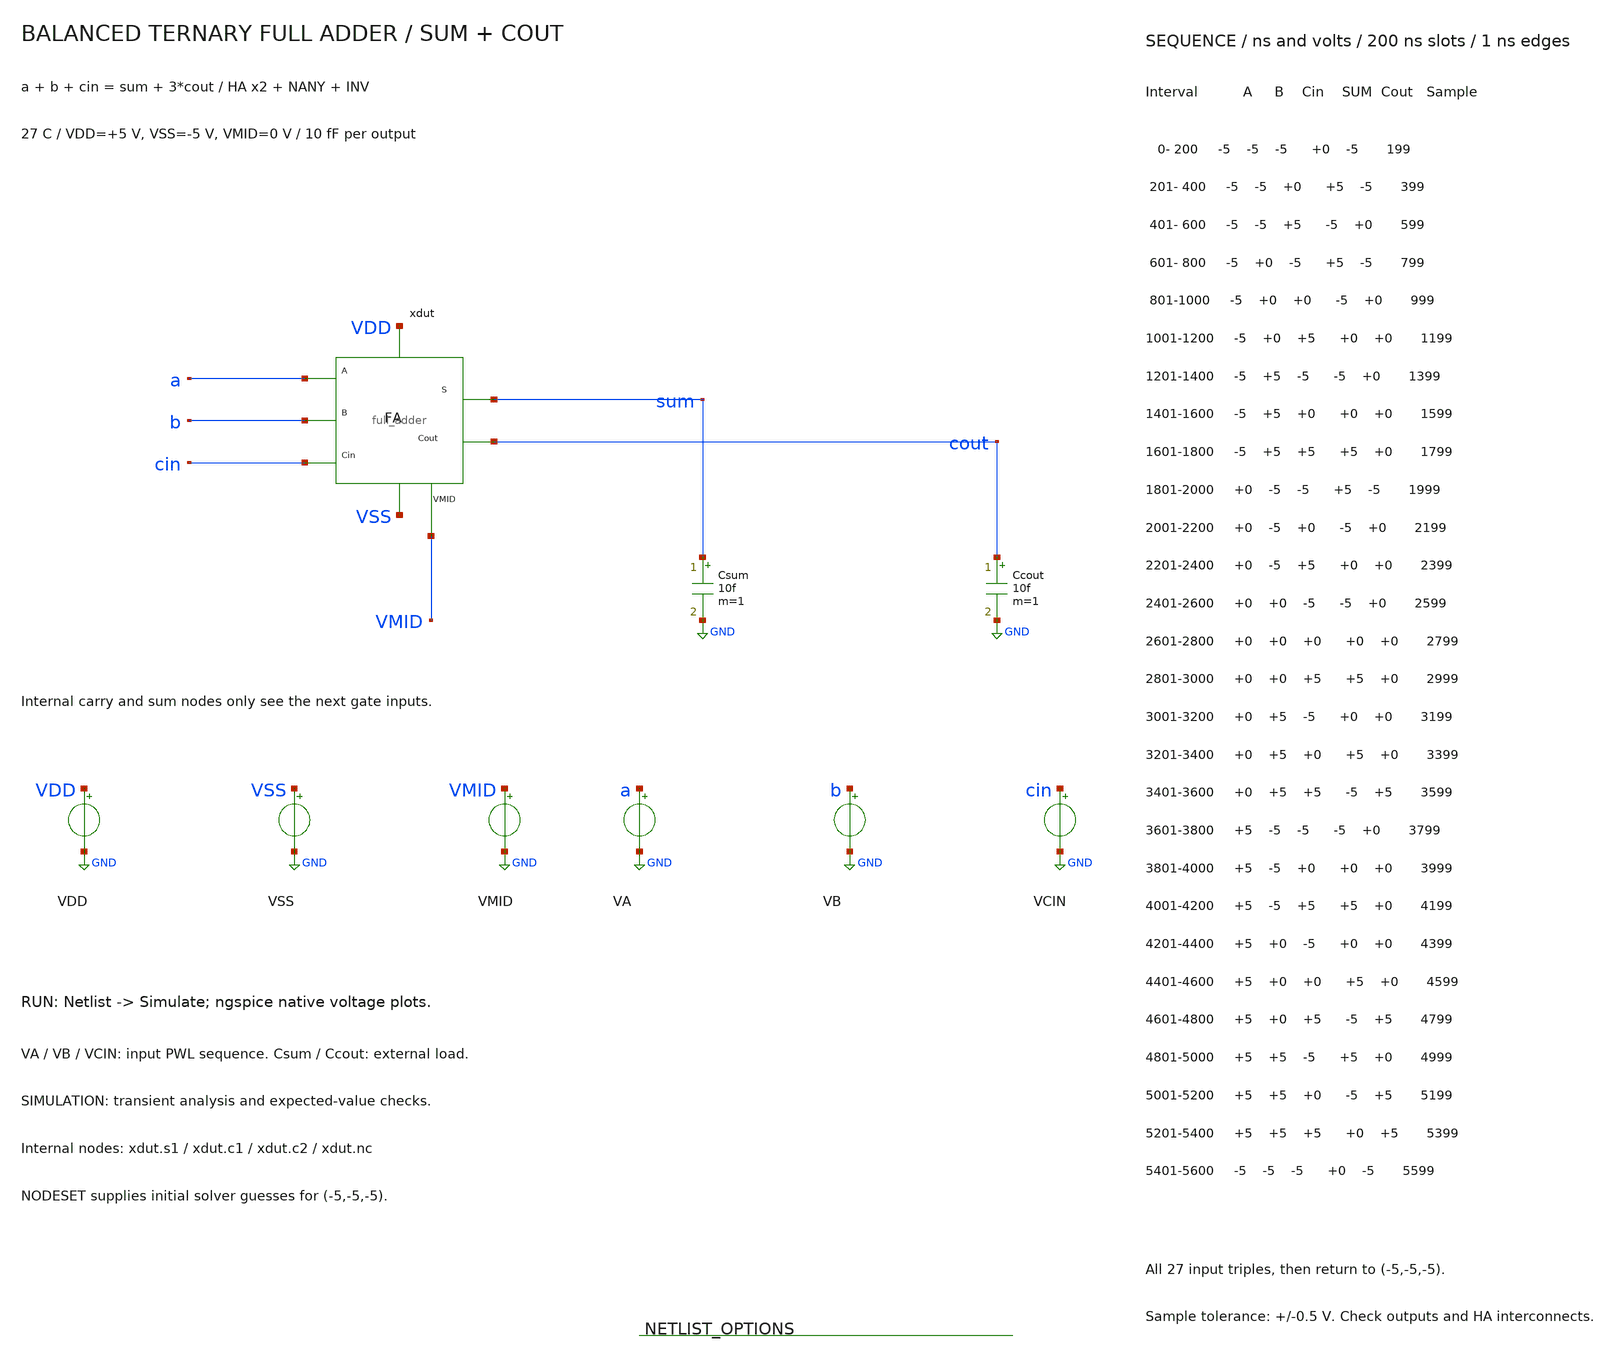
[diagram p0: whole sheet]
** sch_path: member_project/balanced-ternary-logic/PenguinEino/full_adder_tb.sch
**.subckt full_adder_tb
xdut a b cin sum cout VDD VSS VMID full_adder
Csum sum GND 10f m=1
Ccout cout GND 10f m=1
VDD VDD GND 5
VSS VSS GND -5
VMID VMID GND 0
VA a GND PWL(0 -5 200n -5 201n -5 400n -5 401n -5 600n -5 601n -5 800n -5 801n -5 1000n -5 1001n -5
+ 1200n -5 1201n -5 1400n -5 1401n -5 1600n -5 1601n -5 1800n -5 1801n 0 2000n 0 2001n 0 2200n 0 2201n 0
+ 2400n 0 2401n 0 2600n 0 2601n 0 2800n 0 2801n 0 3000n 0 3001n 0 3200n 0 3201n 0 3400n 0 3401n 0 3600n 0
+ 3601n 5 3800n 5 3801n 5 4000n 5 4001n 5 4200n 5 4201n 5 4400n 5 4401n 5 4600n 5 4601n 5 4800n 5 4801n 5
+ 5000n 5 5001n 5 5200n 5 5201n 5 5400n 5 5401n -5 5600n -5)
VB b GND PWL(0 -5 200n -5 201n -5 400n -5 401n -5 600n -5 601n 0 800n 0 801n 0 1000n 0 1001n 0 1200n
+ 0 1201n 5 1400n 5 1401n 5 1600n 5 1601n 5 1800n 5 1801n -5 2000n -5 2001n -5 2200n -5 2201n -5 2400n
+ -5 2401n 0 2600n 0 2601n 0 2800n 0 2801n 0 3000n 0 3001n 5 3200n 5 3201n 5 3400n 5 3401n 5 3600n 5
+ 3601n -5 3800n -5 3801n -5 4000n -5 4001n -5 4200n -5 4201n 0 4400n 0 4401n 0 4600n 0 4601n 0 4800n 0
+ 4801n 5 5000n 5 5001n 5 5200n 5 5201n 5 5400n 5 5401n -5 5600n -5)
VCIN cin GND PWL(0 -5 200n -5 201n 0 400n 0 401n 5 600n 5 601n -5 800n -5 801n 0 1000n 0 1001n 5
+ 1200n 5 1201n -5 1400n -5 1401n 0 1600n 0 1601n 5 1800n 5 1801n -5 2000n -5 2001n 0 2200n 0 2201n 5 2400n
+ 5 2401n -5 2600n -5 2601n 0 2800n 0 2801n 5 3000n 5 3001n -5 3200n -5 3201n 0 3400n 0 3401n 5 3600n 5
+ 3601n -5 3800n -5 3801n 0 4000n 0 4001n 5 4200n 5 4201n -5 4400n -5 4401n 0 4600n 0 4601n 5 4800n 5 4801n
+ -5 5000n -5 5001n 0 5200n 0 5201n 5 5400n 5 5401n -5 5600n -5)
**** begin user architecture code
 .include $::LIB/ip62_models

.temp 27
.options rshunt=1e12
.nodeset v(xdut.s1)=5 v(xdut.c1)=-5 v(xdut.c2)=0 v(xdut.nc)=5 v(sum)=0 v(cout)=-5
.nodeset v(xdut.x_ha1.t)=5 v(xdut.x_ha1.u)=0 v(xdut.x_ha1.na)=5 v(xdut.x_ha1.d)=0 v(xdut.x_ha1.nd)=0
.nodeset v(xdut.x_ha1.x_t.net1)=5 v(xdut.x_ha1.x_t.net2)=5 v(xdut.x_ha1.x_t.net3)=-5
+ v(xdut.x_ha1.x_t.net4)=-5 v(xdut.x_ha1.x_t.net5)=0 v(xdut.x_ha1.x_t.net6)=0
.nodeset v(xdut.x_ha1.x_u.net1)=5 v(xdut.x_ha1.x_u.net2)=5 v(xdut.x_ha1.x_u.net3)=-5
+ v(xdut.x_ha1.x_u.net4)=-5 v(xdut.x_ha1.x_u.net5)=0 v(xdut.x_ha1.x_u.net6)=0
.nodeset v(xdut.x_ha1.x_c.net1)=5 v(xdut.x_ha1.x_c.net2)=5 v(xdut.x_ha1.x_c.net3)=-5
+ v(xdut.x_ha1.x_c.net4)=-5 v(xdut.x_ha1.x_c.net5)=0 v(xdut.x_ha1.x_c.net6)=0
.nodeset v(xdut.x_ha1.x_d.net1)=5 v(xdut.x_ha1.x_d.net2)=5 v(xdut.x_ha1.x_d.net3)=-5
+ v(xdut.x_ha1.x_d.net4)=-5 v(xdut.x_ha1.x_d.net5)=0 v(xdut.x_ha1.x_d.net6)=0
.nodeset v(xdut.x_ha1.x_s.net1)=5 v(xdut.x_ha1.x_s.net2)=5 v(xdut.x_ha1.x_s.net3)=-5
+ v(xdut.x_ha1.x_s.net4)=-5 v(xdut.x_ha1.x_s.net5)=0 v(xdut.x_ha1.x_s.net6)=0
.nodeset v(xdut.x_ha1.x_na.net1)=5 v(xdut.x_ha1.x_na.net2)=-5
.nodeset v(xdut.x_ha1.x_nd.net1)=5 v(xdut.x_ha1.x_nd.net2)=-5
.nodeset v(xdut.x_ha2.t)=0 v(xdut.x_ha2.u)=5 v(xdut.x_ha2.na)=-5 v(xdut.x_ha2.d)=0
+ v(xdut.x_ha2.nd)=0
.nodeset v(xdut.x_ha2.x_t.net1)=5 v(xdut.x_ha2.x_t.net2)=5 v(xdut.x_ha2.x_t.net3)=-5
+ v(xdut.x_ha2.x_t.net4)=-5 v(xdut.x_ha2.x_t.net5)=0 v(xdut.x_ha2.x_t.net6)=0
.nodeset v(xdut.x_ha2.x_u.net1)=5 v(xdut.x_ha2.x_u.net2)=5 v(xdut.x_ha2.x_u.net3)=-5
+ v(xdut.x_ha2.x_u.net4)=-5 v(xdut.x_ha2.x_u.net5)=0 v(xdut.x_ha2.x_u.net6)=0
.nodeset v(xdut.x_ha2.x_c.net1)=5 v(xdut.x_ha2.x_c.net2)=5 v(xdut.x_ha2.x_c.net3)=-5
+ v(xdut.x_ha2.x_c.net4)=-5 v(xdut.x_ha2.x_c.net5)=0 v(xdut.x_ha2.x_c.net6)=0
.nodeset v(xdut.x_ha2.x_d.net1)=5 v(xdut.x_ha2.x_d.net2)=5 v(xdut.x_ha2.x_d.net3)=-5
+ v(xdut.x_ha2.x_d.net4)=-5 v(xdut.x_ha2.x_d.net5)=0 v(xdut.x_ha2.x_d.net6)=0
.nodeset v(xdut.x_ha2.x_s.net1)=5 v(xdut.x_ha2.x_s.net2)=5 v(xdut.x_ha2.x_s.net3)=-5
+ v(xdut.x_ha2.x_s.net4)=-5 v(xdut.x_ha2.x_s.net5)=0 v(xdut.x_ha2.x_s.net6)=0
.nodeset v(xdut.x_ha2.x_na.net1)=5 v(xdut.x_ha2.x_na.net2)=-5
.nodeset v(xdut.x_ha2.x_nd.net1)=5 v(xdut.x_ha2.x_nd.net2)=-5
.nodeset v(xdut.x_cmerge.net1)=5 v(xdut.x_cmerge.net2)=5 v(xdut.x_cmerge.net3)=-5
+ v(xdut.x_cmerge.net4)=-5 v(xdut.x_cmerge.net5)=0 v(xdut.x_cmerge.net6)=0
.nodeset v(xdut.x_cout.net1)=5 v(xdut.x_cout.net2)=-5
.control
save all
set wr_singlescale
set wr_vecnames
setplot const
let failures=0
tran 0.5n 5600n 0 0.5n
plot v(a) v(b) v(cin) v(sum) ylimit -5.5 5.5 title 'Full Adder SUM'
plot v(a) v(b) v(cin) v(cout) ylimit -5.5 5.5 title 'Full Adder COUT'
wrdata full_adder_tran.txt v(a) v(b) v(cin) v(sum) v(cout) v(xdut.s1) v(xdut.c1) v(xdut.c2)
+ v(xdut.nc)
meas tran tran_00_sum find v(sum) at=199n
if abs(tran_00_sum-(0)) > 0.5
let const.failures=const.failures+1
echo FAIL: tran_00_sum expected 0 V
end
meas tran tran_00_cout find v(cout) at=199n
if abs(tran_00_cout-(-5)) > 0.5
let const.failures=const.failures+1
echo FAIL: tran_00_cout expected -5 V
end
meas tran tran_00_xdut_s1 find v(xdut.s1) at=199n
if abs(tran_00_xdut_s1-(5)) > 0.5
let const.failures=const.failures+1
echo FAIL: tran_00_xdut_s1 expected 5 V
end
meas tran tran_00_xdut_c1 find v(xdut.c1) at=199n
if abs(tran_00_xdut_c1-(-5)) > 0.5
let const.failures=const.failures+1
echo FAIL: tran_00_xdut_c1 expected -5 V
end
meas tran tran_00_xdut_c2 find v(xdut.c2) at=199n
if abs(tran_00_xdut_c2-(0)) > 0.5
let const.failures=const.failures+1
echo FAIL: tran_00_xdut_c2 expected 0 V
end
meas tran tran_00_xdut_nc find v(xdut.nc) at=199n
if abs(tran_00_xdut_nc-(5)) > 0.5
let const.failures=const.failures+1
echo FAIL: tran_00_xdut_nc expected 5 V
end
meas tran tran_01_sum find v(sum) at=399n
if abs(tran_01_sum-(5)) > 0.5
let const.failures=const.failures+1
echo FAIL: tran_01_sum expected 5 V
end
meas tran tran_01_cout find v(cout) at=399n
if abs(tran_01_cout-(-5)) > 0.5
let const.failures=const.failures+1
echo FAIL: tran_01_cout expected -5 V
end
meas tran tran_01_xdut_s1 find v(xdut.s1) at=399n
if abs(tran_01_xdut_s1-(5)) > 0.5
let const.failures=const.failures+1
echo FAIL: tran_01_xdut_s1 expected 5 V
end
meas tran tran_01_xdut_c1 find v(xdut.c1) at=399n
if abs(tran_01_xdut_c1-(-5)) > 0.5
let const.failures=const.failures+1
echo FAIL: tran_01_xdut_c1 expected -5 V
end
meas tran tran_01_xdut_c2 find v(xdut.c2) at=399n
if abs(tran_01_xdut_c2-(0)) > 0.5
let const.failures=const.failures+1
echo FAIL: tran_01_xdut_c2 expected 0 V
end
meas tran tran_01_xdut_nc find v(xdut.nc) at=399n
if abs(tran_01_xdut_nc-(5)) > 0.5
let const.failures=const.failures+1
echo FAIL: tran_01_xdut_nc expected 5 V
end
meas tran tran_02_sum find v(sum) at=599n
if abs(tran_02_sum-(-5)) > 0.5
let const.failures=const.failures+1
echo FAIL: tran_02_sum expected -5 V
end
meas tran tran_02_cout find v(cout) at=599n
if abs(tran_02_cout-(0)) > 0.5
let const.failures=const.failures+1
echo FAIL: tran_02_cout expected 0 V
end
meas tran tran_02_xdut_s1 find v(xdut.s1) at=599n
if abs(tran_02_xdut_s1-(5)) > 0.5
let const.failures=const.failures+1
echo FAIL: tran_02_xdut_s1 expected 5 V
end
meas tran tran_02_xdut_c1 find v(xdut.c1) at=599n
if abs(tran_02_xdut_c1-(-5)) > 0.5
let const.failures=const.failures+1
echo FAIL: tran_02_xdut_c1 expected -5 V
end
meas tran tran_02_xdut_c2 find v(xdut.c2) at=599n
if abs(tran_02_xdut_c2-(5)) > 0.5
let const.failures=const.failures+1
echo FAIL: tran_02_xdut_c2 expected 5 V
end
meas tran tran_02_xdut_nc find v(xdut.nc) at=599n
if abs(tran_02_xdut_nc-(0)) > 0.5
let const.failures=const.failures+1
echo FAIL: tran_02_xdut_nc expected 0 V
end
meas tran tran_03_sum find v(sum) at=799n
if abs(tran_03_sum-(5)) > 0.5
let const.failures=const.failures+1
echo FAIL: tran_03_sum expected 5 V
end
meas tran tran_03_cout find v(cout) at=799n
if abs(tran_03_cout-(-5)) > 0.5
let const.failures=const.failures+1
echo FAIL: tran_03_cout expected -5 V
end
meas tran tran_03_xdut_s1 find v(xdut.s1) at=799n
if abs(tran_03_xdut_s1-(-5)) > 0.5
let const.failures=const.failures+1
echo FAIL: tran_03_xdut_s1 expected -5 V
end
meas tran tran_03_xdut_c1 find v(xdut.c1) at=799n
if abs(tran_03_xdut_c1-(0)) > 0.5
let const.failures=const.failures+1
echo FAIL: tran_03_xdut_c1 expected 0 V
end
meas tran tran_03_xdut_c2 find v(xdut.c2) at=799n
if abs(tran_03_xdut_c2-(-5)) > 0.5
let const.failures=const.failures+1
echo FAIL: tran_03_xdut_c2 expected -5 V
end
meas tran tran_03_xdut_nc find v(xdut.nc) at=799n
if abs(tran_03_xdut_nc-(5)) > 0.5
let const.failures=const.failures+1
echo FAIL: tran_03_xdut_nc expected 5 V
end
meas tran tran_04_sum find v(sum) at=999n
if abs(tran_04_sum-(-5)) > 0.5
let const.failures=const.failures+1
echo FAIL: tran_04_sum expected -5 V
end
meas tran tran_04_cout find v(cout) at=999n
if abs(tran_04_cout-(0)) > 0.5
let const.failures=const.failures+1
echo FAIL: tran_04_cout expected 0 V
end
meas tran tran_04_xdut_s1 find v(xdut.s1) at=999n
if abs(tran_04_xdut_s1-(-5)) > 0.5
let const.failures=const.failures+1
echo FAIL: tran_04_xdut_s1 expected -5 V
end
meas tran tran_04_xdut_c1 find v(xdut.c1) at=999n
if abs(tran_04_xdut_c1-(0)) > 0.5
let const.failures=const.failures+1
echo FAIL: tran_04_xdut_c1 expected 0 V
end
meas tran tran_04_xdut_c2 find v(xdut.c2) at=999n
if abs(tran_04_xdut_c2-(0)) > 0.5
let const.failures=const.failures+1
echo FAIL: tran_04_xdut_c2 expected 0 V
end
meas tran tran_04_xdut_nc find v(xdut.nc) at=999n
if abs(tran_04_xdut_nc-(0)) > 0.5
let const.failures=const.failures+1
echo FAIL: tran_04_xdut_nc expected 0 V
end
meas tran tran_05_sum find v(sum) at=1199n
if abs(tran_05_sum-(0)) > 0.5
let const.failures=const.failures+1
echo FAIL: tran_05_sum expected 0 V
end
meas tran tran_05_cout find v(cout) at=1199n
if abs(tran_05_cout-(0)) > 0.5
let const.failures=const.failures+1
echo FAIL: tran_05_cout expected 0 V
end
meas tran tran_05_xdut_s1 find v(xdut.s1) at=1199n
if abs(tran_05_xdut_s1-(-5)) > 0.5
let const.failures=const.failures+1
echo FAIL: tran_05_xdut_s1 expected -5 V
end
meas tran tran_05_xdut_c1 find v(xdut.c1) at=1199n
if abs(tran_05_xdut_c1-(0)) > 0.5
let const.failures=const.failures+1
echo FAIL: tran_05_xdut_c1 expected 0 V
end
meas tran tran_05_xdut_c2 find v(xdut.c2) at=1199n
if abs(tran_05_xdut_c2-(0)) > 0.5
let const.failures=const.failures+1
echo FAIL: tran_05_xdut_c2 expected 0 V
end
meas tran tran_05_xdut_nc find v(xdut.nc) at=1199n
if abs(tran_05_xdut_nc-(0)) > 0.5
let const.failures=const.failures+1
echo FAIL: tran_05_xdut_nc expected 0 V
end
meas tran tran_06_sum find v(sum) at=1399n
if abs(tran_06_sum-(-5)) > 0.5
let const.failures=const.failures+1
echo FAIL: tran_06_sum expected -5 V
end
meas tran tran_06_cout find v(cout) at=1399n
if abs(tran_06_cout-(0)) > 0.5
let const.failures=const.failures+1
echo FAIL: tran_06_cout expected 0 V
end
meas tran tran_06_xdut_s1 find v(xdut.s1) at=1399n
if abs(tran_06_xdut_s1-(0)) > 0.5
let const.failures=const.failures+1
echo FAIL: tran_06_xdut_s1 expected 0 V
end
meas tran tran_06_xdut_c1 find v(xdut.c1) at=1399n
if abs(tran_06_xdut_c1-(0)) > 0.5
let const.failures=const.failures+1
echo FAIL: tran_06_xdut_c1 expected 0 V
end
meas tran tran_06_xdut_c2 find v(xdut.c2) at=1399n
if abs(tran_06_xdut_c2-(0)) > 0.5
let const.failures=const.failures+1
echo FAIL: tran_06_xdut_c2 expected 0 V
end
meas tran tran_06_xdut_nc find v(xdut.nc) at=1399n
if abs(tran_06_xdut_nc-(0)) > 0.5
let const.failures=const.failures+1
echo FAIL: tran_06_xdut_nc expected 0 V
end
meas tran tran_07_sum find v(sum) at=1599n
if abs(tran_07_sum-(0)) > 0.5
let const.failures=const.failures+1
echo FAIL: tran_07_sum expected 0 V
end
meas tran tran_07_cout find v(cout) at=1599n
if abs(tran_07_cout-(0)) > 0.5
let const.failures=const.failures+1
echo FAIL: tran_07_cout expected 0 V
end
meas tran tran_07_xdut_s1 find v(xdut.s1) at=1599n
if abs(tran_07_xdut_s1-(0)) > 0.5
let const.failures=const.failures+1
echo FAIL: tran_07_xdut_s1 expected 0 V
end
meas tran tran_07_xdut_c1 find v(xdut.c1) at=1599n
if abs(tran_07_xdut_c1-(0)) > 0.5
let const.failures=const.failures+1
echo FAIL: tran_07_xdut_c1 expected 0 V
end
meas tran tran_07_xdut_c2 find v(xdut.c2) at=1599n
if abs(tran_07_xdut_c2-(0)) > 0.5
let const.failures=const.failures+1
echo FAIL: tran_07_xdut_c2 expected 0 V
end
meas tran tran_07_xdut_nc find v(xdut.nc) at=1599n
if abs(tran_07_xdut_nc-(0)) > 0.5
let const.failures=const.failures+1
echo FAIL: tran_07_xdut_nc expected 0 V
end
meas tran tran_08_sum find v(sum) at=1799n
if abs(tran_08_sum-(5)) > 0.5
let const.failures=const.failures+1
echo FAIL: tran_08_sum expected 5 V
end
meas tran tran_08_cout find v(cout) at=1799n
if abs(tran_08_cout-(0)) > 0.5
let const.failures=const.failures+1
echo FAIL: tran_08_cout expected 0 V
end
meas tran tran_08_xdut_s1 find v(xdut.s1) at=1799n
if abs(tran_08_xdut_s1-(0)) > 0.5
let const.failures=const.failures+1
echo FAIL: tran_08_xdut_s1 expected 0 V
end
meas tran tran_08_xdut_c1 find v(xdut.c1) at=1799n
if abs(tran_08_xdut_c1-(0)) > 0.5
let const.failures=const.failures+1
echo FAIL: tran_08_xdut_c1 expected 0 V
end
meas tran tran_08_xdut_c2 find v(xdut.c2) at=1799n
if abs(tran_08_xdut_c2-(0)) > 0.5
let const.failures=const.failures+1
echo FAIL: tran_08_xdut_c2 expected 0 V
end
meas tran tran_08_xdut_nc find v(xdut.nc) at=1799n
if abs(tran_08_xdut_nc-(0)) > 0.5
let const.failures=const.failures+1
echo FAIL: tran_08_xdut_nc expected 0 V
end
meas tran tran_09_sum find v(sum) at=1999n
if abs(tran_09_sum-(5)) > 0.5
let const.failures=const.failures+1
echo FAIL: tran_09_sum expected 5 V
end
meas tran tran_09_cout find v(cout) at=1999n
if abs(tran_09_cout-(-5)) > 0.5
let const.failures=const.failures+1
echo FAIL: tran_09_cout expected -5 V
end
meas tran tran_09_xdut_s1 find v(xdut.s1) at=1999n
if abs(tran_09_xdut_s1-(-5)) > 0.5
let const.failures=const.failures+1
echo FAIL: tran_09_xdut_s1 expected -5 V
end
meas tran tran_09_xdut_c1 find v(xdut.c1) at=1999n
if abs(tran_09_xdut_c1-(0)) > 0.5
let const.failures=const.failures+1
echo FAIL: tran_09_xdut_c1 expected 0 V
end
meas tran tran_09_xdut_c2 find v(xdut.c2) at=1999n
if abs(tran_09_xdut_c2-(-5)) > 0.5
let const.failures=const.failures+1
echo FAIL: tran_09_xdut_c2 expected -5 V
end
meas tran tran_09_xdut_nc find v(xdut.nc) at=1999n
if abs(tran_09_xdut_nc-(5)) > 0.5
let const.failures=const.failures+1
echo FAIL: tran_09_xdut_nc expected 5 V
end
meas tran tran_10_sum find v(sum) at=2199n
if abs(tran_10_sum-(-5)) > 0.5
let const.failures=const.failures+1
echo FAIL: tran_10_sum expected -5 V
end
meas tran tran_10_cout find v(cout) at=2199n
if abs(tran_10_cout-(0)) > 0.5
let const.failures=const.failures+1
echo FAIL: tran_10_cout expected 0 V
end
meas tran tran_10_xdut_s1 find v(xdut.s1) at=2199n
if abs(tran_10_xdut_s1-(-5)) > 0.5
let const.failures=const.failures+1
echo FAIL: tran_10_xdut_s1 expected -5 V
end
meas tran tran_10_xdut_c1 find v(xdut.c1) at=2199n
if abs(tran_10_xdut_c1-(0)) > 0.5
let const.failures=const.failures+1
echo FAIL: tran_10_xdut_c1 expected 0 V
end
meas tran tran_10_xdut_c2 find v(xdut.c2) at=2199n
if abs(tran_10_xdut_c2-(0)) > 0.5
let const.failures=const.failures+1
echo FAIL: tran_10_xdut_c2 expected 0 V
end
meas tran tran_10_xdut_nc find v(xdut.nc) at=2199n
if abs(tran_10_xdut_nc-(0)) > 0.5
let const.failures=const.failures+1
echo FAIL: tran_10_xdut_nc expected 0 V
end
meas tran tran_11_sum find v(sum) at=2399n
if abs(tran_11_sum-(0)) > 0.5
let const.failures=const.failures+1
echo FAIL: tran_11_sum expected 0 V
end
meas tran tran_11_cout find v(cout) at=2399n
if abs(tran_11_cout-(0)) > 0.5
let const.failures=const.failures+1
echo FAIL: tran_11_cout expected 0 V
end
meas tran tran_11_xdut_s1 find v(xdut.s1) at=2399n
if abs(tran_11_xdut_s1-(-5)) > 0.5
let const.failures=const.failures+1
echo FAIL: tran_11_xdut_s1 expected -5 V
end
meas tran tran_11_xdut_c1 find v(xdut.c1) at=2399n
if abs(tran_11_xdut_c1-(0)) > 0.5
let const.failures=const.failures+1
echo FAIL: tran_11_xdut_c1 expected 0 V
end
meas tran tran_11_xdut_c2 find v(xdut.c2) at=2399n
if abs(tran_11_xdut_c2-(0)) > 0.5
let const.failures=const.failures+1
echo FAIL: tran_11_xdut_c2 expected 0 V
end
meas tran tran_11_xdut_nc find v(xdut.nc) at=2399n
if abs(tran_11_xdut_nc-(0)) > 0.5
let const.failures=const.failures+1
echo FAIL: tran_11_xdut_nc expected 0 V
end
meas tran tran_12_sum find v(sum) at=2599n
if abs(tran_12_sum-(-5)) > 0.5
let const.failures=const.failures+1
echo FAIL: tran_12_sum expected -5 V
end
meas tran tran_12_cout find v(cout) at=2599n
if abs(tran_12_cout-(0)) > 0.5
let const.failures=const.failures+1
echo FAIL: tran_12_cout expected 0 V
end
meas tran tran_12_xdut_s1 find v(xdut.s1) at=2599n
if abs(tran_12_xdut_s1-(0)) > 0.5
let const.failures=const.failures+1
echo FAIL: tran_12_xdut_s1 expected 0 V
end
meas tran tran_12_xdut_c1 find v(xdut.c1) at=2599n
if abs(tran_12_xdut_c1-(0)) > 0.5
let const.failures=const.failures+1
echo FAIL: tran_12_xdut_c1 expected 0 V
end
meas tran tran_12_xdut_c2 find v(xdut.c2) at=2599n
if abs(tran_12_xdut_c2-(0)) > 0.5
let const.failures=const.failures+1
echo FAIL: tran_12_xdut_c2 expected 0 V
end
meas tran tran_12_xdut_nc find v(xdut.nc) at=2599n
if abs(tran_12_xdut_nc-(0)) > 0.5
let const.failures=const.failures+1
echo FAIL: tran_12_xdut_nc expected 0 V
end
meas tran tran_13_sum find v(sum) at=2799n
if abs(tran_13_sum-(0)) > 0.5
let const.failures=const.failures+1
echo FAIL: tran_13_sum expected 0 V
end
meas tran tran_13_cout find v(cout) at=2799n
if abs(tran_13_cout-(0)) > 0.5
let const.failures=const.failures+1
echo FAIL: tran_13_cout expected 0 V
end
meas tran tran_13_xdut_s1 find v(xdut.s1) at=2799n
if abs(tran_13_xdut_s1-(0)) > 0.5
let const.failures=const.failures+1
echo FAIL: tran_13_xdut_s1 expected 0 V
end
meas tran tran_13_xdut_c1 find v(xdut.c1) at=2799n
if abs(tran_13_xdut_c1-(0)) > 0.5
let const.failures=const.failures+1
echo FAIL: tran_13_xdut_c1 expected 0 V
end
meas tran tran_13_xdut_c2 find v(xdut.c2) at=2799n
if abs(tran_13_xdut_c2-(0)) > 0.5
let const.failures=const.failures+1
echo FAIL: tran_13_xdut_c2 expected 0 V
end
meas tran tran_13_xdut_nc find v(xdut.nc) at=2799n
if abs(tran_13_xdut_nc-(0)) > 0.5
let const.failures=const.failures+1
echo FAIL: tran_13_xdut_nc expected 0 V
end
meas tran tran_14_sum find v(sum) at=2999n
if abs(tran_14_sum-(5)) > 0.5
let const.failures=const.failures+1
echo FAIL: tran_14_sum expected 5 V
end
meas tran tran_14_cout find v(cout) at=2999n
if abs(tran_14_cout-(0)) > 0.5
let const.failures=const.failures+1
echo FAIL: tran_14_cout expected 0 V
end
meas tran tran_14_xdut_s1 find v(xdut.s1) at=2999n
if abs(tran_14_xdut_s1-(0)) > 0.5
let const.failures=const.failures+1
echo FAIL: tran_14_xdut_s1 expected 0 V
end
meas tran tran_14_xdut_c1 find v(xdut.c1) at=2999n
if abs(tran_14_xdut_c1-(0)) > 0.5
let const.failures=const.failures+1
echo FAIL: tran_14_xdut_c1 expected 0 V
end
meas tran tran_14_xdut_c2 find v(xdut.c2) at=2999n
if abs(tran_14_xdut_c2-(0)) > 0.5
let const.failures=const.failures+1
echo FAIL: tran_14_xdut_c2 expected 0 V
end
meas tran tran_14_xdut_nc find v(xdut.nc) at=2999n
if abs(tran_14_xdut_nc-(0)) > 0.5
let const.failures=const.failures+1
echo FAIL: tran_14_xdut_nc expected 0 V
end
meas tran tran_15_sum find v(sum) at=3199n
if abs(tran_15_sum-(0)) > 0.5
let const.failures=const.failures+1
echo FAIL: tran_15_sum expected 0 V
end
meas tran tran_15_cout find v(cout) at=3199n
if abs(tran_15_cout-(0)) > 0.5
let const.failures=const.failures+1
echo FAIL: tran_15_cout expected 0 V
end
meas tran tran_15_xdut_s1 find v(xdut.s1) at=3199n
if abs(tran_15_xdut_s1-(5)) > 0.5
let const.failures=const.failures+1
echo FAIL: tran_15_xdut_s1 expected 5 V
end
meas tran tran_15_xdut_c1 find v(xdut.c1) at=3199n
if abs(tran_15_xdut_c1-(0)) > 0.5
let const.failures=const.failures+1
echo FAIL: tran_15_xdut_c1 expected 0 V
end
meas tran tran_15_xdut_c2 find v(xdut.c2) at=3199n
if abs(tran_15_xdut_c2-(0)) > 0.5
let const.failures=const.failures+1
echo FAIL: tran_15_xdut_c2 expected 0 V
end
meas tran tran_15_xdut_nc find v(xdut.nc) at=3199n
if abs(tran_15_xdut_nc-(0)) > 0.5
let const.failures=const.failures+1
echo FAIL: tran_15_xdut_nc expected 0 V
end
meas tran tran_16_sum find v(sum) at=3399n
if abs(tran_16_sum-(5)) > 0.5
let const.failures=const.failures+1
echo FAIL: tran_16_sum expected 5 V
end
meas tran tran_16_cout find v(cout) at=3399n
if abs(tran_16_cout-(0)) > 0.5
let const.failures=const.failures+1
echo FAIL: tran_16_cout expected 0 V
end
meas tran tran_16_xdut_s1 find v(xdut.s1) at=3399n
if abs(tran_16_xdut_s1-(5)) > 0.5
let const.failures=const.failures+1
echo FAIL: tran_16_xdut_s1 expected 5 V
end
meas tran tran_16_xdut_c1 find v(xdut.c1) at=3399n
if abs(tran_16_xdut_c1-(0)) > 0.5
let const.failures=const.failures+1
echo FAIL: tran_16_xdut_c1 expected 0 V
end
meas tran tran_16_xdut_c2 find v(xdut.c2) at=3399n
if abs(tran_16_xdut_c2-(0)) > 0.5
let const.failures=const.failures+1
echo FAIL: tran_16_xdut_c2 expected 0 V
end
meas tran tran_16_xdut_nc find v(xdut.nc) at=3399n
if abs(tran_16_xdut_nc-(0)) > 0.5
let const.failures=const.failures+1
echo FAIL: tran_16_xdut_nc expected 0 V
end
meas tran tran_17_sum find v(sum) at=3599n
if abs(tran_17_sum-(-5)) > 0.5
let const.failures=const.failures+1
echo FAIL: tran_17_sum expected -5 V
end
meas tran tran_17_cout find v(cout) at=3599n
if abs(tran_17_cout-(5)) > 0.5
let const.failures=const.failures+1
echo FAIL: tran_17_cout expected 5 V
end
meas tran tran_17_xdut_s1 find v(xdut.s1) at=3599n
if abs(tran_17_xdut_s1-(5)) > 0.5
let const.failures=const.failures+1
echo FAIL: tran_17_xdut_s1 expected 5 V
end
meas tran tran_17_xdut_c1 find v(xdut.c1) at=3599n
if abs(tran_17_xdut_c1-(0)) > 0.5
let const.failures=const.failures+1
echo FAIL: tran_17_xdut_c1 expected 0 V
end
meas tran tran_17_xdut_c2 find v(xdut.c2) at=3599n
if abs(tran_17_xdut_c2-(5)) > 0.5
let const.failures=const.failures+1
echo FAIL: tran_17_xdut_c2 expected 5 V
end
meas tran tran_17_xdut_nc find v(xdut.nc) at=3599n
if abs(tran_17_xdut_nc-(-5)) > 0.5
let const.failures=const.failures+1
echo FAIL: tran_17_xdut_nc expected -5 V
end
meas tran tran_18_sum find v(sum) at=3799n
if abs(tran_18_sum-(-5)) > 0.5
let const.failures=const.failures+1
echo FAIL: tran_18_sum expected -5 V
end
meas tran tran_18_cout find v(cout) at=3799n
if abs(tran_18_cout-(0)) > 0.5
let const.failures=const.failures+1
echo FAIL: tran_18_cout expected 0 V
end
meas tran tran_18_xdut_s1 find v(xdut.s1) at=3799n
if abs(tran_18_xdut_s1-(0)) > 0.5
let const.failures=const.failures+1
echo FAIL: tran_18_xdut_s1 expected 0 V
end
meas tran tran_18_xdut_c1 find v(xdut.c1) at=3799n
if abs(tran_18_xdut_c1-(0)) > 0.5
let const.failures=const.failures+1
echo FAIL: tran_18_xdut_c1 expected 0 V
end
meas tran tran_18_xdut_c2 find v(xdut.c2) at=3799n
if abs(tran_18_xdut_c2-(0)) > 0.5
let const.failures=const.failures+1
echo FAIL: tran_18_xdut_c2 expected 0 V
end
meas tran tran_18_xdut_nc find v(xdut.nc) at=3799n
if abs(tran_18_xdut_nc-(0)) > 0.5
let const.failures=const.failures+1
echo FAIL: tran_18_xdut_nc expected 0 V
end
meas tran tran_19_sum find v(sum) at=3999n
if abs(tran_19_sum-(0)) > 0.5
let const.failures=const.failures+1
echo FAIL: tran_19_sum expected 0 V
end
meas tran tran_19_cout find v(cout) at=3999n
if abs(tran_19_cout-(0)) > 0.5
let const.failures=const.failures+1
echo FAIL: tran_19_cout expected 0 V
end
meas tran tran_19_xdut_s1 find v(xdut.s1) at=3999n
if abs(tran_19_xdut_s1-(0)) > 0.5
let const.failures=const.failures+1
echo FAIL: tran_19_xdut_s1 expected 0 V
end
meas tran tran_19_xdut_c1 find v(xdut.c1) at=3999n
if abs(tran_19_xdut_c1-(0)) > 0.5
let const.failures=const.failures+1
echo FAIL: tran_19_xdut_c1 expected 0 V
end
meas tran tran_19_xdut_c2 find v(xdut.c2) at=3999n
if abs(tran_19_xdut_c2-(0)) > 0.5
let const.failures=const.failures+1
echo FAIL: tran_19_xdut_c2 expected 0 V
end
meas tran tran_19_xdut_nc find v(xdut.nc) at=3999n
if abs(tran_19_xdut_nc-(0)) > 0.5
let const.failures=const.failures+1
echo FAIL: tran_19_xdut_nc expected 0 V
end
meas tran tran_20_sum find v(sum) at=4199n
if abs(tran_20_sum-(5)) > 0.5
let const.failures=const.failures+1
echo FAIL: tran_20_sum expected 5 V
end
meas tran tran_20_cout find v(cout) at=4199n
if abs(tran_20_cout-(0)) > 0.5
let const.failures=const.failures+1
echo FAIL: tran_20_cout expected 0 V
end
meas tran tran_20_xdut_s1 find v(xdut.s1) at=4199n
if abs(tran_20_xdut_s1-(0)) > 0.5
let const.failures=const.failures+1
echo FAIL: tran_20_xdut_s1 expected 0 V
end
meas tran tran_20_xdut_c1 find v(xdut.c1) at=4199n
if abs(tran_20_xdut_c1-(0)) > 0.5
let const.failures=const.failures+1
echo FAIL: tran_20_xdut_c1 expected 0 V
end
meas tran tran_20_xdut_c2 find v(xdut.c2) at=4199n
if abs(tran_20_xdut_c2-(0)) > 0.5
let const.failures=const.failures+1
echo FAIL: tran_20_xdut_c2 expected 0 V
end
meas tran tran_20_xdut_nc find v(xdut.nc) at=4199n
if abs(tran_20_xdut_nc-(0)) > 0.5
let const.failures=const.failures+1
echo FAIL: tran_20_xdut_nc expected 0 V
end
meas tran tran_21_sum find v(sum) at=4399n
if abs(tran_21_sum-(0)) > 0.5
let const.failures=const.failures+1
echo FAIL: tran_21_sum expected 0 V
end
meas tran tran_21_cout find v(cout) at=4399n
if abs(tran_21_cout-(0)) > 0.5
let const.failures=const.failures+1
echo FAIL: tran_21_cout expected 0 V
end
meas tran tran_21_xdut_s1 find v(xdut.s1) at=4399n
if abs(tran_21_xdut_s1-(5)) > 0.5
let const.failures=const.failures+1
echo FAIL: tran_21_xdut_s1 expected 5 V
end
meas tran tran_21_xdut_c1 find v(xdut.c1) at=4399n
if abs(tran_21_xdut_c1-(0)) > 0.5
let const.failures=const.failures+1
echo FAIL: tran_21_xdut_c1 expected 0 V
end
meas tran tran_21_xdut_c2 find v(xdut.c2) at=4399n
if abs(tran_21_xdut_c2-(0)) > 0.5
let const.failures=const.failures+1
echo FAIL: tran_21_xdut_c2 expected 0 V
end
meas tran tran_21_xdut_nc find v(xdut.nc) at=4399n
if abs(tran_21_xdut_nc-(0)) > 0.5
let const.failures=const.failures+1
echo FAIL: tran_21_xdut_nc expected 0 V
end
meas tran tran_22_sum find v(sum) at=4599n
if abs(tran_22_sum-(5)) > 0.5
let const.failures=const.failures+1
echo FAIL: tran_22_sum expected 5 V
end
meas tran tran_22_cout find v(cout) at=4599n
if abs(tran_22_cout-(0)) > 0.5
let const.failures=const.failures+1
echo FAIL: tran_22_cout expected 0 V
end
meas tran tran_22_xdut_s1 find v(xdut.s1) at=4599n
if abs(tran_22_xdut_s1-(5)) > 0.5
let const.failures=const.failures+1
echo FAIL: tran_22_xdut_s1 expected 5 V
end
meas tran tran_22_xdut_c1 find v(xdut.c1) at=4599n
if abs(tran_22_xdut_c1-(0)) > 0.5
let const.failures=const.failures+1
echo FAIL: tran_22_xdut_c1 expected 0 V
end
meas tran tran_22_xdut_c2 find v(xdut.c2) at=4599n
if abs(tran_22_xdut_c2-(0)) > 0.5
let const.failures=const.failures+1
echo FAIL: tran_22_xdut_c2 expected 0 V
end
meas tran tran_22_xdut_nc find v(xdut.nc) at=4599n
if abs(tran_22_xdut_nc-(0)) > 0.5
let const.failures=const.failures+1
echo FAIL: tran_22_xdut_nc expected 0 V
end
meas tran tran_23_sum find v(sum) at=4799n
if abs(tran_23_sum-(-5)) > 0.5
let const.failures=const.failures+1
echo FAIL: tran_23_sum expected -5 V
end
meas tran tran_23_cout find v(cout) at=4799n
if abs(tran_23_cout-(5)) > 0.5
let const.failures=const.failures+1
echo FAIL: tran_23_cout expected 5 V
end
meas tran tran_23_xdut_s1 find v(xdut.s1) at=4799n
if abs(tran_23_xdut_s1-(5)) > 0.5
let const.failures=const.failures+1
echo FAIL: tran_23_xdut_s1 expected 5 V
end
meas tran tran_23_xdut_c1 find v(xdut.c1) at=4799n
if abs(tran_23_xdut_c1-(0)) > 0.5
let const.failures=const.failures+1
echo FAIL: tran_23_xdut_c1 expected 0 V
end
meas tran tran_23_xdut_c2 find v(xdut.c2) at=4799n
if abs(tran_23_xdut_c2-(5)) > 0.5
let const.failures=const.failures+1
echo FAIL: tran_23_xdut_c2 expected 5 V
end
meas tran tran_23_xdut_nc find v(xdut.nc) at=4799n
if abs(tran_23_xdut_nc-(-5)) > 0.5
let const.failures=const.failures+1
echo FAIL: tran_23_xdut_nc expected -5 V
end
meas tran tran_24_sum find v(sum) at=4999n
if abs(tran_24_sum-(5)) > 0.5
let const.failures=const.failures+1
echo FAIL: tran_24_sum expected 5 V
end
meas tran tran_24_cout find v(cout) at=4999n
if abs(tran_24_cout-(0)) > 0.5
let const.failures=const.failures+1
echo FAIL: tran_24_cout expected 0 V
end
meas tran tran_24_xdut_s1 find v(xdut.s1) at=4999n
if abs(tran_24_xdut_s1-(-5)) > 0.5
let const.failures=const.failures+1
echo FAIL: tran_24_xdut_s1 expected -5 V
end
meas tran tran_24_xdut_c1 find v(xdut.c1) at=4999n
if abs(tran_24_xdut_c1-(5)) > 0.5
let const.failures=const.failures+1
echo FAIL: tran_24_xdut_c1 expected 5 V
end
meas tran tran_24_xdut_c2 find v(xdut.c2) at=4999n
if abs(tran_24_xdut_c2-(-5)) > 0.5
let const.failures=const.failures+1
echo FAIL: tran_24_xdut_c2 expected -5 V
end
meas tran tran_24_xdut_nc find v(xdut.nc) at=4999n
if abs(tran_24_xdut_nc-(0)) > 0.5
let const.failures=const.failures+1
echo FAIL: tran_24_xdut_nc expected 0 V
end
meas tran tran_25_sum find v(sum) at=5199n
if abs(tran_25_sum-(-5)) > 0.5
let const.failures=const.failures+1
echo FAIL: tran_25_sum expected -5 V
end
meas tran tran_25_cout find v(cout) at=5199n
if abs(tran_25_cout-(5)) > 0.5
let const.failures=const.failures+1
echo FAIL: tran_25_cout expected 5 V
end
meas tran tran_25_xdut_s1 find v(xdut.s1) at=5199n
if abs(tran_25_xdut_s1-(-5)) > 0.5
let const.failures=const.failures+1
echo FAIL: tran_25_xdut_s1 expected -5 V
end
meas tran tran_25_xdut_c1 find v(xdut.c1) at=5199n
if abs(tran_25_xdut_c1-(5)) > 0.5
let const.failures=const.failures+1
echo FAIL: tran_25_xdut_c1 expected 5 V
end
meas tran tran_25_xdut_c2 find v(xdut.c2) at=5199n
if abs(tran_25_xdut_c2-(0)) > 0.5
let const.failures=const.failures+1
echo FAIL: tran_25_xdut_c2 expected 0 V
end
meas tran tran_25_xdut_nc find v(xdut.nc) at=5199n
if abs(tran_25_xdut_nc-(-5)) > 0.5
let const.failures=const.failures+1
echo FAIL: tran_25_xdut_nc expected -5 V
end
meas tran tran_26_sum find v(sum) at=5399n
if abs(tran_26_sum-(0)) > 0.5
let const.failures=const.failures+1
echo FAIL: tran_26_sum expected 0 V
end
meas tran tran_26_cout find v(cout) at=5399n
if abs(tran_26_cout-(5)) > 0.5
let const.failures=const.failures+1
echo FAIL: tran_26_cout expected 5 V
end
meas tran tran_26_xdut_s1 find v(xdut.s1) at=5399n
if abs(tran_26_xdut_s1-(-5)) > 0.5
let const.failures=const.failures+1
echo FAIL: tran_26_xdut_s1 expected -5 V
end
meas tran tran_26_xdut_c1 find v(xdut.c1) at=5399n
if abs(tran_26_xdut_c1-(5)) > 0.5
let const.failures=const.failures+1
echo FAIL: tran_26_xdut_c1 expected 5 V
end
meas tran tran_26_xdut_c2 find v(xdut.c2) at=5399n
if abs(tran_26_xdut_c2-(0)) > 0.5
let const.failures=const.failures+1
echo FAIL: tran_26_xdut_c2 expected 0 V
end
meas tran tran_26_xdut_nc find v(xdut.nc) at=5399n
if abs(tran_26_xdut_nc-(-5)) > 0.5
let const.failures=const.failures+1
echo FAIL: tran_26_xdut_nc expected -5 V
end
meas tran tran_27_sum find v(sum) at=5599n
if abs(tran_27_sum-(0)) > 0.5
let const.failures=const.failures+1
echo FAIL: tran_27_sum expected 0 V
end
meas tran tran_27_cout find v(cout) at=5599n
if abs(tran_27_cout-(-5)) > 0.5
let const.failures=const.failures+1
echo FAIL: tran_27_cout expected -5 V
end
meas tran tran_27_xdut_s1 find v(xdut.s1) at=5599n
if abs(tran_27_xdut_s1-(5)) > 0.5
let const.failures=const.failures+1
echo FAIL: tran_27_xdut_s1 expected 5 V
end
meas tran tran_27_xdut_c1 find v(xdut.c1) at=5599n
if abs(tran_27_xdut_c1-(-5)) > 0.5
let const.failures=const.failures+1
echo FAIL: tran_27_xdut_c1 expected -5 V
end
meas tran tran_27_xdut_c2 find v(xdut.c2) at=5599n
if abs(tran_27_xdut_c2-(0)) > 0.5
let const.failures=const.failures+1
echo FAIL: tran_27_xdut_c2 expected 0 V
end
meas tran tran_27_xdut_nc find v(xdut.nc) at=5599n
if abs(tran_27_xdut_nc-(5)) > 0.5
let const.failures=const.failures+1
echo FAIL: tran_27_xdut_nc expected 5 V
end
if const.failures = 0
echo PASS: Full Adder 27 triples plus return; SUM/COUT and internal interconnects
else
echo FAIL: Full Adder samples outside +/-0.5 V
end
print const.failures
.endc

**** end user architecture code
**.ends

* expanding   symbol:  /home/ishi-kai/balanced-ternary-logic/full_adder.sym # of pins=8
** sym_path: member_project/balanced-ternary-logic/PenguinEino/submission/full_adder.sym
** sch_path: member_project/balanced-ternary-logic/PenguinEino/submission/full_adder.sch
.subckt full_adder a b cin sum cout VDD VSS VMID
*.ipin a
*.ipin b
*.ipin cin
*.opin sum
*.opin cout
*.iopin VDD
*.iopin VSS
*.iopin VMID
x_ha1 a b s1 c1 VDD VSS VMID half_adder
x_ha2 s1 cin sum c2 VDD VSS VMID half_adder
x_cmerge c1 c2 nc VDD VSS VMID nany
x_cout nc cout VDD VSS inverter
.ends


* expanding   symbol:  half_adder.sym # of pins=7
** sym_path: member_project/balanced-ternary-logic/PenguinEino/half_adder.sym
** sch_path: member_project/balanced-ternary-logic/PenguinEino/half_adder.sch
.subckt half_adder a b sum carry VDD VSS VMID
*.ipin a
*.ipin b
*.opin carry
*.iopin VDD
*.iopin VSS
*.iopin VMID
*.opin sum
x_t a b t VDD VSS VMID nany
x_u b t u VDD VSS VMID nany
x_na a na VDD VSS inverter
x_c na u carry VDD VSS VMID nany
x_d t carry d VDD VSS VMID nany
x_nd d nd VDD VSS inverter
x_s nd carry sum VDD VSS VMID nany
.ends


* expanding   symbol:  nany.sym # of pins=6
** sym_path: member_project/balanced-ternary-logic/PenguinEino/submission/nany.sym
** sch_path: member_project/balanced-ternary-logic/PenguinEino/submission/nany.sch
.subckt nany a b vout VDD VSS VMID
*.iopin VDD
*.ipin a
*.ipin b
*.opin vout
*.iopin VSS
*.iopin VMID
XXM3 net2 b net1 VDD PMOS w=34u l=1u nrd=0 nrs=0 m=1
XR2 net2 vout VDD F_RR w=2.8e-06 l=30e-06 R=1 tc1=0 tc2=0 m=1
XR1 vout net3 VDD F_RR w=2.8e-06 l=30e-06 R=1 tc1=0 tc2=0 m=1
XXM2 net3 a net4 VSS NMOS w=11u l=1u nrd=0 nrs=0 m=1
XXM1 net4 b VSS VSS NMOS w=11u l=1u nrd=0 nrs=0 m=1
XXM5 net1 a VDD VDD PMOS w=34u l=1u nrd=0 nrs=0 m=1
XXM6 net5 a vout VDD PMOS w=14u l=1u nrd=0 nrs=0 m=1
XXM7 net5 b VMID VSS NMOS w=8u l=1u nrd=0 nrs=0 m=1
XXM8 net6 b vout VDD PMOS w=14u l=1u nrd=0 nrs=0 m=1
XXM9 net6 a VMID VSS NMOS w=8u l=1u nrd=0 nrs=0 m=1
.ends


* expanding   symbol:  inverter.sym # of pins=4
** sym_path: member_project/balanced-ternary-logic/PenguinEino/inverter.sym
** sch_path: member_project/balanced-ternary-logic/PenguinEino/inverter.sch
.subckt inverter vin vout VDD VSS
*.iopin VDD
*.ipin vin
*.opin vout
*.iopin VSS
XXM1 net1 vin VDD VDD PMOS w=13.5u l=1u nrd=0 nrs=0 m=1
XR1 net1 vout VDD F_RR w=2.8e-06 l=30e-06 R=1 tc1=0 tc2=0 m=1
XR2 vout net2 VDD F_RR w=2.8e-06 l=30e-06 R=1 tc1=0 tc2=0 m=1
XXM2 net2 vin VSS VSS NMOS w=5u l=1u nrd=0 nrs=0 m=1
.ends

.GLOBAL GND
.end
